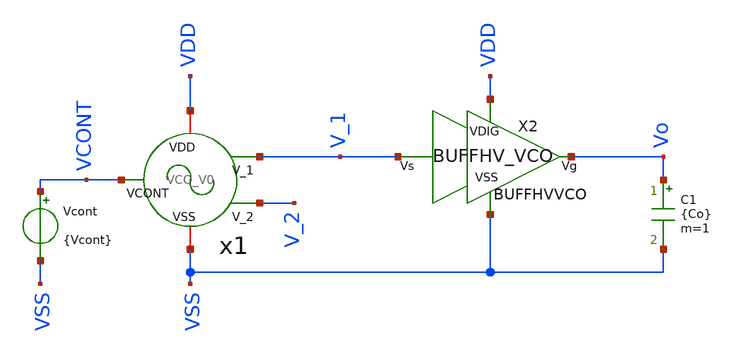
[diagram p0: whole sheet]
** sch_path: xschem/VCO/TB_VCO_V0.sch
**.subckt TB_VCO_V0
C1 Vo VSS {Co} m=1
Vcont VCONT VSS {Vcont}
X2 V_1 Vo VDD VSS BUFFHVVCO
x1 VCONT VSS VDD V_1 V_2 VCO_V0
**** begin user architecture code

.param Co = 1p
.param mult = 1
.param w_inv = 0.15u
.param l_inv = 0.15u

*.param Vcont = 0.8
.param VCP = 0.57
.param VCN = 0.76

vvdd vdd 0 dc 3.3
vvss vss 0 0
*vvcont VCONT 0 dc 0
*vvcont2 VCONT2 0 dc 0
*.option temp = 200
.ic v(V_1) = 0
.ic v(V_2) = 3.3
*.ic v(V_11) = 0
*.ic v(V_22) = 3.3
.save v(V_1) v(Vo)

.param fmin = 7.5Meg
*.param fmin = 1Meg
.param Tmin = 1/fmin
.param SimTime =  Tmin*20
.csparam SimTime ={Simtime}
.csparam Tmargin = Tmin*2





.param Vo = 0
.param Vref = Vo*2/3.3
.param Vcont = Vref

.save all
.tran 5n {SimTime}
*.tran 10n 1u
.csparam start = 10
.control
let Vtarg = 1.5
let f_sum = 0
let t_act = 0
let period_cont = 3
let period_cont2 = 4
run
meas tran T TRIG v(Vo) VAL = {Vtarg} RISE = {period_cont} TARG v(Vo) VAL = {Vtarg}  RISE = {period_cont2}
meas tran VCN AVG v(x1.x1.VCN) FROM=0 TO={SimTime}
meas tran VCP AVG v(x1.x1.VCP) FROM=0 TO={SimTime}
let f =1/T
plot v(Vo)
plot v(x1.x1.VCN) v(x1.x1.VCP)
plot i(v.x1.x1.VIcont)
print f VCN VCP
.endc




.lib cornerMOShv.lib mos_tt
.lib cornerMOSlv.lib mos_tt
*.lib cornerMOShv.lib mos_ff
*.lib cornerMOSlv.lib mos_ff
*.lib cornerMOShv.lib mos_ss
*.lib cornerMOSlv.lib mos_ss
*.lib cornerMOShv.lib mos_sf
*.lib cornerMOSlv.lib mos_sf
*.lib cornerMOShv.lib mos_fs
*.lib cornerMOSlv.lib mos_fs

*.include /opt/pdks/ihp-sg13g2/libs.ref/sg13g2_stdcell/spice/sg13g2_stdcell.spice
*.lib $::SG13G2_MODELS/cornerRES.lib res_typ
*.lib $::SG13G2_MODELS/cornerCAP.lib cap_typ
*.lib $::SG13G2_MODELS/diodes.lib




.option KLU
*.option itl4=100
.option method=gear
*.option maxord=2
*.option trtol=25
*.option lvltim=1
*.option tnum=1e9
*.option reltol=1e-3
*.option abstol=1e-10
*.option vntol=1e-4
*.option event
*.option gmin=1e-10
*.option cshunt=1e-13




.param w_MP1a = 2u
.param l_MP1a = 7u
.param w_MP1b = 1u
.param l_MP1b = 7u
.param w_MP2 = 8u
.param l_MP2 = 4u
.param w_MP3 = 5u
.param l_MP3 = 4u
.param w_MP4 = 5u
.param l_MP4 = 5u

.param w_MN1 = 5u
.param l_MN1 = 0.5u
.param w_MN2 = 5u
.param l_MN2 = 0.5u
.param w_MN3 = 3u
.param l_MN3 = 0.5u
.param w_MN4 = 2u
.param l_MN4 = 5u




**** end user architecture code
**.ends
.end
